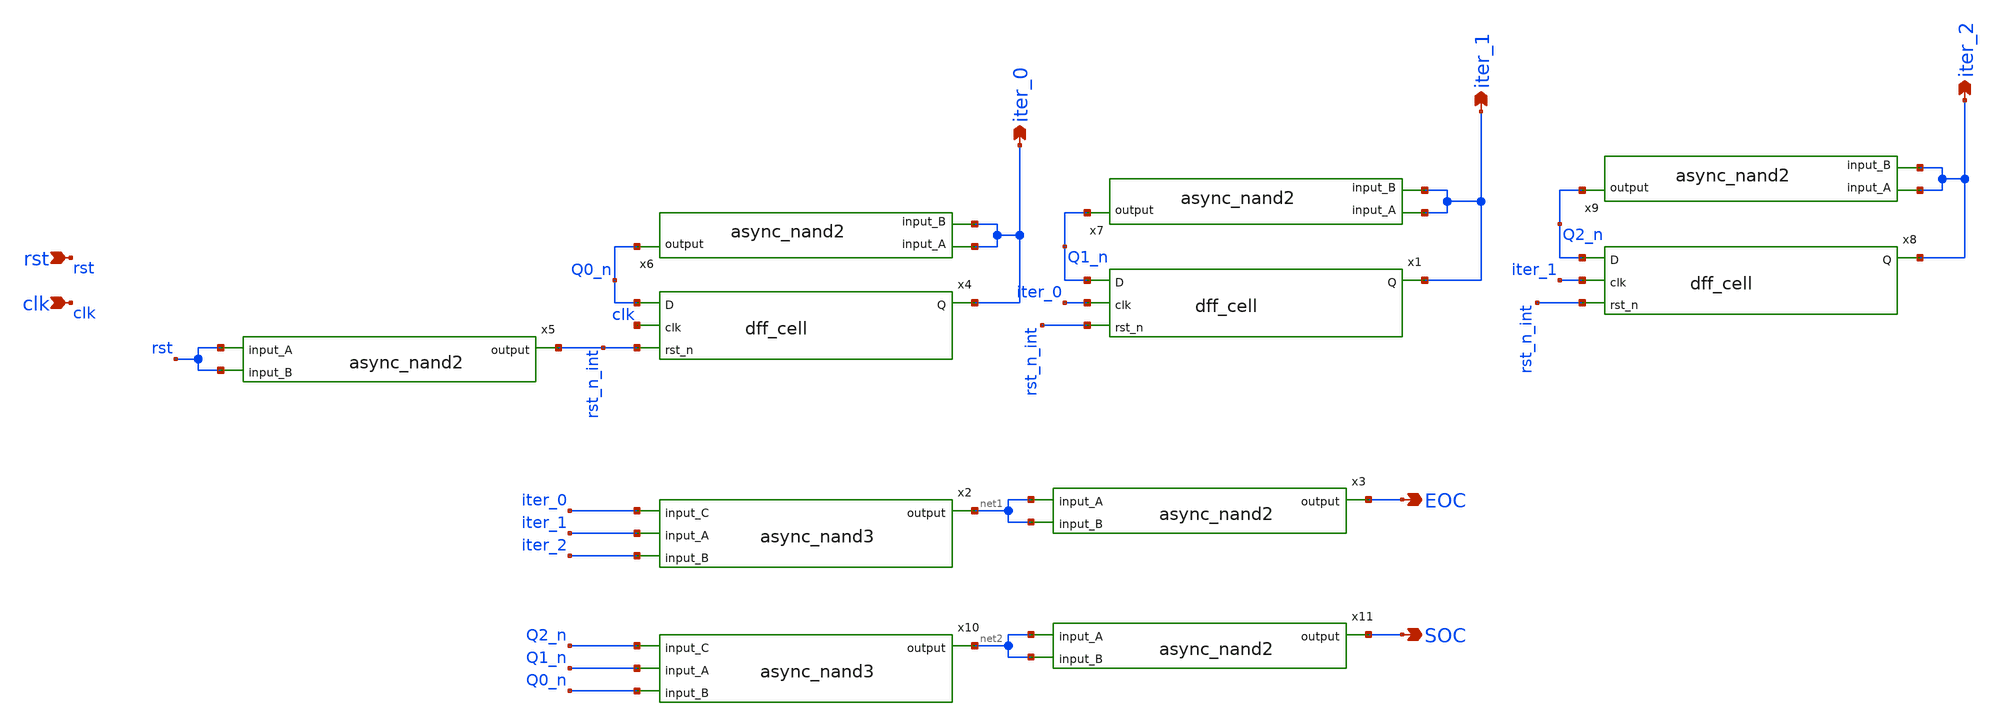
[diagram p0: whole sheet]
** sch_path: xschem/sar_adc/soc_eoc.sch
**.subckt soc_eoc clk rst iter_0 EOC iter_1 iter_2 SOC
*.ipin clk
*.ipin rst
*.opin iter_0
*.opin EOC
*.opin iter_1
*.opin iter_2
*.opin SOC
x5 rst rst_n_int rst async_nand2
x4 Q0_n clk rst_n_int iter_0 dff_cell
x6 iter_0 Q0_n iter_0 async_nand2
x1 Q1_n iter_0 rst_n_int iter_1 dff_cell
x7 iter_1 Q1_n iter_1 async_nand2
x8 Q2_n iter_1 rst_n_int iter_2 dff_cell
x9 iter_2 Q2_n iter_2 async_nand2
x2 iter_0 iter_1 iter_2 net1 async_nand3
x3 net1 EOC net1 async_nand2
x10 Q2_n Q1_n Q0_n net2 async_nand3
x11 net2 SOC net2 async_nand2
**.ends
.end
